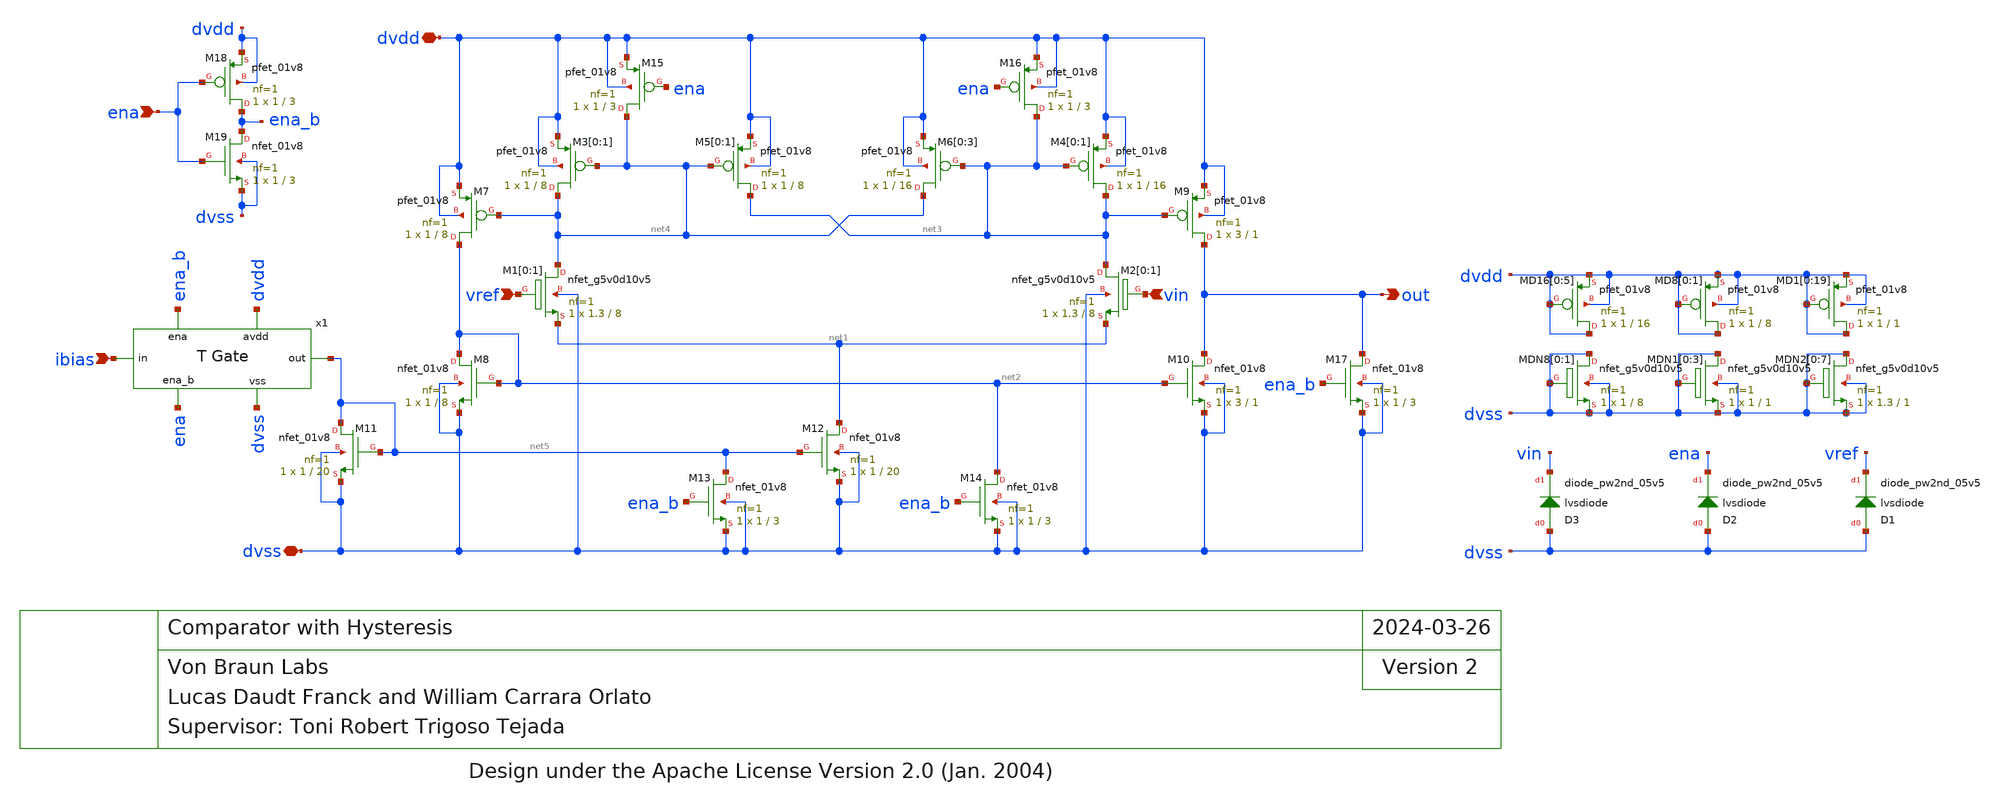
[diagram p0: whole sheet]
** sch_path: xschem/comp_hyst.sch
* Design under the Apache License Version 2.0 (Jan. 2004)
**.subckt comp_hyst dvdd vref vin out ibias ena dvss
*.iopin dvdd
*.ipin vref
*.ipin vin
*.opin out
*.ipin ibias
*.ipin ena
*.iopin dvss
XM5[0] net3 net4 dvdd dvdd sky130_fd_pr__pfet_01v8 L=8 W=1 nf=1 ad='int((nf+1)/2) * W/nf * 0.29' as='int((nf+2)/2) * W/nf * 0.29'
+ pd='2*int((nf+1)/2) * (W/nf + 0.29)' ps='2*int((nf+2)/2) * (W/nf + 0.29)' nrd='0.29 / W' nrs='0.29 / W'
+ sa=0 sb=0 sd=0 mult=1 m=1
XM5[1] net3 net4 dvdd dvdd sky130_fd_pr__pfet_01v8 L=8 W=1 nf=1 ad='int((nf+1)/2) * W/nf * 0.29' as='int((nf+2)/2) * W/nf * 0.29'
+ pd='2*int((nf+1)/2) * (W/nf + 0.29)' ps='2*int((nf+2)/2) * (W/nf + 0.29)' nrd='0.29 / W' nrs='0.29 / W'
+ sa=0 sb=0 sd=0 mult=1 m=1
XM3[0] net4 net4 dvdd dvdd sky130_fd_pr__pfet_01v8 L=8 W=1 nf=1 ad='int((nf+1)/2) * W/nf * 0.29' as='int((nf+2)/2) * W/nf * 0.29'
+ pd='2*int((nf+1)/2) * (W/nf + 0.29)' ps='2*int((nf+2)/2) * (W/nf + 0.29)' nrd='0.29 / W' nrs='0.29 / W'
+ sa=0 sb=0 sd=0 mult=1 m=1
XM3[1] net4 net4 dvdd dvdd sky130_fd_pr__pfet_01v8 L=8 W=1 nf=1 ad='int((nf+1)/2) * W/nf * 0.29' as='int((nf+2)/2) * W/nf * 0.29'
+ pd='2*int((nf+1)/2) * (W/nf + 0.29)' ps='2*int((nf+2)/2) * (W/nf + 0.29)' nrd='0.29 / W' nrs='0.29 / W'
+ sa=0 sb=0 sd=0 mult=1 m=1
XM7 net2 net4 dvdd dvdd sky130_fd_pr__pfet_01v8 L=8 W=1 nf=1 ad='int((nf+1)/2) * W/nf * 0.29' as='int((nf+2)/2) * W/nf * 0.29'
+ pd='2*int((nf+1)/2) * (W/nf + 0.29)' ps='2*int((nf+2)/2) * (W/nf + 0.29)' nrd='0.29 / W' nrs='0.29 / W'
+ sa=0 sb=0 sd=0 mult=1 m=1
XM4[0] net3 net3 dvdd dvdd sky130_fd_pr__pfet_01v8 L=16 W=1 nf=1 ad='int((nf+1)/2) * W/nf * 0.29' as='int((nf+2)/2) * W/nf * 0.29'
+ pd='2*int((nf+1)/2) * (W/nf + 0.29)' ps='2*int((nf+2)/2) * (W/nf + 0.29)' nrd='0.29 / W' nrs='0.29 / W'
+ sa=0 sb=0 sd=0 mult=1 m=1
XM4[1] net3 net3 dvdd dvdd sky130_fd_pr__pfet_01v8 L=16 W=1 nf=1 ad='int((nf+1)/2) * W/nf * 0.29' as='int((nf+2)/2) * W/nf * 0.29'
+ pd='2*int((nf+1)/2) * (W/nf + 0.29)' ps='2*int((nf+2)/2) * (W/nf + 0.29)' nrd='0.29 / W' nrs='0.29 / W'
+ sa=0 sb=0 sd=0 mult=1 m=1
XM11 net5 net5 dvss dvss sky130_fd_pr__nfet_01v8 L=20 W=1 nf=1 ad='int((nf+1)/2) * W/nf * 0.29' as='int((nf+2)/2) * W/nf * 0.29'
+ pd='2*int((nf+1)/2) * (W/nf + 0.29)' ps='2*int((nf+2)/2) * (W/nf + 0.29)' nrd='0.29 / W' nrs='0.29 / W'
+ sa=0 sb=0 sd=0 mult=1 m=1
XM12 net1 net5 dvss dvss sky130_fd_pr__nfet_01v8 L=20 W=1 nf=1 ad='int((nf+1)/2) * W/nf * 0.29' as='int((nf+2)/2) * W/nf * 0.29'
+ pd='2*int((nf+1)/2) * (W/nf + 0.29)' ps='2*int((nf+2)/2) * (W/nf + 0.29)' nrd='0.29 / W' nrs='0.29 / W'
+ sa=0 sb=0 sd=0 mult=1 m=1
XM9 out net3 dvdd dvdd sky130_fd_pr__pfet_01v8 L=1 W=3 nf=1 ad='int((nf+1)/2) * W/nf * 0.29' as='int((nf+2)/2) * W/nf * 0.29'
+ pd='2*int((nf+1)/2) * (W/nf + 0.29)' ps='2*int((nf+2)/2) * (W/nf + 0.29)' nrd='0.29 / W' nrs='0.29 / W'
+ sa=0 sb=0 sd=0 mult=1 m=1
XM10 out net2 dvss dvss sky130_fd_pr__nfet_01v8 L=1 W=3 nf=1 ad='int((nf+1)/2) * W/nf * 0.29' as='int((nf+2)/2) * W/nf * 0.29'
+ pd='2*int((nf+1)/2) * (W/nf + 0.29)' ps='2*int((nf+2)/2) * (W/nf + 0.29)' nrd='0.29 / W' nrs='0.29 / W'
+ sa=0 sb=0 sd=0 mult=1 m=1
XM17 out ena_b dvss dvss sky130_fd_pr__nfet_01v8 L=3 W=1 nf=1 ad='int((nf+1)/2) * W/nf * 0.29' as='int((nf+2)/2) * W/nf * 0.29'
+ pd='2*int((nf+1)/2) * (W/nf + 0.29)' ps='2*int((nf+2)/2) * (W/nf + 0.29)' nrd='0.29 / W' nrs='0.29 / W'
+ sa=0 sb=0 sd=0 mult=1 m=1
XM1[0] net4 vref net1 dvss sky130_fd_pr__nfet_g5v0d10v5 L=8 W=1.3 nf=1 ad='int((nf+1)/2) * W/nf * 0.29'
+ as='int((nf+2)/2) * W/nf * 0.29' pd='2*int((nf+1)/2) * (W/nf + 0.29)' ps='2*int((nf+2)/2) * (W/nf + 0.29)'
+ nrd='0.29 / W' nrs='0.29 / W' sa=0 sb=0 sd=0 mult=1 m=1
XM1[1] net4 vref net1 dvss sky130_fd_pr__nfet_g5v0d10v5 L=8 W=1.3 nf=1 ad='int((nf+1)/2) * W/nf * 0.29'
+ as='int((nf+2)/2) * W/nf * 0.29' pd='2*int((nf+1)/2) * (W/nf + 0.29)' ps='2*int((nf+2)/2) * (W/nf + 0.29)'
+ nrd='0.29 / W' nrs='0.29 / W' sa=0 sb=0 sd=0 mult=1 m=1
XM2[0] net3 vin net1 dvss sky130_fd_pr__nfet_g5v0d10v5 L=8 W=1.3 nf=1 ad='int((nf+1)/2) * W/nf * 0.29'
+ as='int((nf+2)/2) * W/nf * 0.29' pd='2*int((nf+1)/2) * (W/nf + 0.29)' ps='2*int((nf+2)/2) * (W/nf + 0.29)'
+ nrd='0.29 / W' nrs='0.29 / W' sa=0 sb=0 sd=0 mult=1 m=1
XM2[1] net3 vin net1 dvss sky130_fd_pr__nfet_g5v0d10v5 L=8 W=1.3 nf=1 ad='int((nf+1)/2) * W/nf * 0.29'
+ as='int((nf+2)/2) * W/nf * 0.29' pd='2*int((nf+1)/2) * (W/nf + 0.29)' ps='2*int((nf+2)/2) * (W/nf + 0.29)'
+ nrd='0.29 / W' nrs='0.29 / W' sa=0 sb=0 sd=0 mult=1 m=1
XM13 net5 ena_b dvss dvss sky130_fd_pr__nfet_01v8 L=3 W=1 nf=1 ad='int((nf+1)/2) * W/nf * 0.29' as='int((nf+2)/2) * W/nf * 0.29'
+ pd='2*int((nf+1)/2) * (W/nf + 0.29)' ps='2*int((nf+2)/2) * (W/nf + 0.29)' nrd='0.29 / W' nrs='0.29 / W'
+ sa=0 sb=0 sd=0 mult=1 m=1
XM6[0] net4 net3 dvdd dvdd sky130_fd_pr__pfet_01v8 L=16 W=1 nf=1 ad='int((nf+1)/2) * W/nf * 0.29' as='int((nf+2)/2) * W/nf * 0.29'
+ pd='2*int((nf+1)/2) * (W/nf + 0.29)' ps='2*int((nf+2)/2) * (W/nf + 0.29)' nrd='0.29 / W' nrs='0.29 / W'
+ sa=0 sb=0 sd=0 mult=1 m=1
XM6[1] net4 net3 dvdd dvdd sky130_fd_pr__pfet_01v8 L=16 W=1 nf=1 ad='int((nf+1)/2) * W/nf * 0.29' as='int((nf+2)/2) * W/nf * 0.29'
+ pd='2*int((nf+1)/2) * (W/nf + 0.29)' ps='2*int((nf+2)/2) * (W/nf + 0.29)' nrd='0.29 / W' nrs='0.29 / W'
+ sa=0 sb=0 sd=0 mult=1 m=1
XM6[2] net4 net3 dvdd dvdd sky130_fd_pr__pfet_01v8 L=16 W=1 nf=1 ad='int((nf+1)/2) * W/nf * 0.29' as='int((nf+2)/2) * W/nf * 0.29'
+ pd='2*int((nf+1)/2) * (W/nf + 0.29)' ps='2*int((nf+2)/2) * (W/nf + 0.29)' nrd='0.29 / W' nrs='0.29 / W'
+ sa=0 sb=0 sd=0 mult=1 m=1
XM6[3] net4 net3 dvdd dvdd sky130_fd_pr__pfet_01v8 L=16 W=1 nf=1 ad='int((nf+1)/2) * W/nf * 0.29' as='int((nf+2)/2) * W/nf * 0.29'
+ pd='2*int((nf+1)/2) * (W/nf + 0.29)' ps='2*int((nf+2)/2) * (W/nf + 0.29)' nrd='0.29 / W' nrs='0.29 / W'
+ sa=0 sb=0 sd=0 mult=1 m=1
XM8 net2 net2 dvss dvss sky130_fd_pr__nfet_01v8 L=8 W=1 nf=1 ad='int((nf+1)/2) * W/nf * 0.29' as='int((nf+2)/2) * W/nf * 0.29'
+ pd='2*int((nf+1)/2) * (W/nf + 0.29)' ps='2*int((nf+2)/2) * (W/nf + 0.29)' nrd='0.29 / W' nrs='0.29 / W'
+ sa=0 sb=0 sd=0 mult=1 m=1
XM16 net3 ena dvdd dvdd sky130_fd_pr__pfet_01v8 L=3 W=1 nf=1 ad='int((nf+1)/2) * W/nf * 0.29' as='int((nf+2)/2) * W/nf * 0.29'
+ pd='2*int((nf+1)/2) * (W/nf + 0.29)' ps='2*int((nf+2)/2) * (W/nf + 0.29)' nrd='0.29 / W' nrs='0.29 / W'
+ sa=0 sb=0 sd=0 mult=1 m=1
XM15 net4 ena dvdd dvdd sky130_fd_pr__pfet_01v8 L=3 W=1 nf=1 ad='int((nf+1)/2) * W/nf * 0.29' as='int((nf+2)/2) * W/nf * 0.29'
+ pd='2*int((nf+1)/2) * (W/nf + 0.29)' ps='2*int((nf+2)/2) * (W/nf + 0.29)' nrd='0.29 / W' nrs='0.29 / W'
+ sa=0 sb=0 sd=0 mult=1 m=1
XM14 net2 ena_b dvss dvss sky130_fd_pr__nfet_01v8 L=3 W=1 nf=1 ad='int((nf+1)/2) * W/nf * 0.29' as='int((nf+2)/2) * W/nf * 0.29'
+ pd='2*int((nf+1)/2) * (W/nf + 0.29)' ps='2*int((nf+2)/2) * (W/nf + 0.29)' nrd='0.29 / W' nrs='0.29 / W'
+ sa=0 sb=0 sd=0 mult=1 m=1
XM18 ena_b ena dvdd dvdd sky130_fd_pr__pfet_01v8 L=3 W=1 nf=1 ad='int((nf+1)/2) * W/nf * 0.29' as='int((nf+2)/2) * W/nf * 0.29'
+ pd='2*int((nf+1)/2) * (W/nf + 0.29)' ps='2*int((nf+2)/2) * (W/nf + 0.29)' nrd='0.29 / W' nrs='0.29 / W'
+ sa=0 sb=0 sd=0 mult=1 m=1
XM19 ena_b ena dvss dvss sky130_fd_pr__nfet_01v8 L=3 W=1 nf=1 ad='int((nf+1)/2) * W/nf * 0.29' as='int((nf+2)/2) * W/nf * 0.29'
+ pd='2*int((nf+1)/2) * (W/nf + 0.29)' ps='2*int((nf+2)/2) * (W/nf + 0.29)' nrd='0.29 / W' nrs='0.29 / W'
+ sa=0 sb=0 sd=0 mult=1 m=1
x1 ibias ena ena_b dvdd dvss net5 trans_gate
XMD16[0] dvdd dvdd dvdd dvdd sky130_fd_pr__pfet_01v8 L=16 W=1 nf=1 ad='int((nf+1)/2) * W/nf * 0.29' as='int((nf+2)/2) * W/nf * 0.29'
+ pd='2*int((nf+1)/2) * (W/nf + 0.29)' ps='2*int((nf+2)/2) * (W/nf + 0.29)' nrd='0.29 / W' nrs='0.29 / W'
+ sa=0 sb=0 sd=0 mult=1 m=1
XMD16[1] dvdd dvdd dvdd dvdd sky130_fd_pr__pfet_01v8 L=16 W=1 nf=1 ad='int((nf+1)/2) * W/nf * 0.29' as='int((nf+2)/2) * W/nf * 0.29'
+ pd='2*int((nf+1)/2) * (W/nf + 0.29)' ps='2*int((nf+2)/2) * (W/nf + 0.29)' nrd='0.29 / W' nrs='0.29 / W'
+ sa=0 sb=0 sd=0 mult=1 m=1
XMD16[2] dvdd dvdd dvdd dvdd sky130_fd_pr__pfet_01v8 L=16 W=1 nf=1 ad='int((nf+1)/2) * W/nf * 0.29' as='int((nf+2)/2) * W/nf * 0.29'
+ pd='2*int((nf+1)/2) * (W/nf + 0.29)' ps='2*int((nf+2)/2) * (W/nf + 0.29)' nrd='0.29 / W' nrs='0.29 / W'
+ sa=0 sb=0 sd=0 mult=1 m=1
XMD16[3] dvdd dvdd dvdd dvdd sky130_fd_pr__pfet_01v8 L=16 W=1 nf=1 ad='int((nf+1)/2) * W/nf * 0.29' as='int((nf+2)/2) * W/nf * 0.29'
+ pd='2*int((nf+1)/2) * (W/nf + 0.29)' ps='2*int((nf+2)/2) * (W/nf + 0.29)' nrd='0.29 / W' nrs='0.29 / W'
+ sa=0 sb=0 sd=0 mult=1 m=1
XMD16[4] dvdd dvdd dvdd dvdd sky130_fd_pr__pfet_01v8 L=16 W=1 nf=1 ad='int((nf+1)/2) * W/nf * 0.29' as='int((nf+2)/2) * W/nf * 0.29'
+ pd='2*int((nf+1)/2) * (W/nf + 0.29)' ps='2*int((nf+2)/2) * (W/nf + 0.29)' nrd='0.29 / W' nrs='0.29 / W'
+ sa=0 sb=0 sd=0 mult=1 m=1
XMD16[5] dvdd dvdd dvdd dvdd sky130_fd_pr__pfet_01v8 L=16 W=1 nf=1 ad='int((nf+1)/2) * W/nf * 0.29' as='int((nf+2)/2) * W/nf * 0.29'
+ pd='2*int((nf+1)/2) * (W/nf + 0.29)' ps='2*int((nf+2)/2) * (W/nf + 0.29)' nrd='0.29 / W' nrs='0.29 / W'
+ sa=0 sb=0 sd=0 mult=1 m=1
XMD8[0] dvdd dvdd dvdd dvdd sky130_fd_pr__pfet_01v8 L=8 W=1 nf=1 ad='int((nf+1)/2) * W/nf * 0.29' as='int((nf+2)/2) * W/nf * 0.29'
+ pd='2*int((nf+1)/2) * (W/nf + 0.29)' ps='2*int((nf+2)/2) * (W/nf + 0.29)' nrd='0.29 / W' nrs='0.29 / W'
+ sa=0 sb=0 sd=0 mult=1 m=1
XMD8[1] dvdd dvdd dvdd dvdd sky130_fd_pr__pfet_01v8 L=8 W=1 nf=1 ad='int((nf+1)/2) * W/nf * 0.29' as='int((nf+2)/2) * W/nf * 0.29'
+ pd='2*int((nf+1)/2) * (W/nf + 0.29)' ps='2*int((nf+2)/2) * (W/nf + 0.29)' nrd='0.29 / W' nrs='0.29 / W'
+ sa=0 sb=0 sd=0 mult=1 m=1
XMD1[0] dvdd dvdd dvdd dvdd sky130_fd_pr__pfet_01v8 L=1 W=1 nf=1 ad='int((nf+1)/2) * W/nf * 0.29' as='int((nf+2)/2) * W/nf * 0.29'
+ pd='2*int((nf+1)/2) * (W/nf + 0.29)' ps='2*int((nf+2)/2) * (W/nf + 0.29)' nrd='0.29 / W' nrs='0.29 / W'
+ sa=0 sb=0 sd=0 mult=1 m=1
XMD1[1] dvdd dvdd dvdd dvdd sky130_fd_pr__pfet_01v8 L=1 W=1 nf=1 ad='int((nf+1)/2) * W/nf * 0.29' as='int((nf+2)/2) * W/nf * 0.29'
+ pd='2*int((nf+1)/2) * (W/nf + 0.29)' ps='2*int((nf+2)/2) * (W/nf + 0.29)' nrd='0.29 / W' nrs='0.29 / W'
+ sa=0 sb=0 sd=0 mult=1 m=1
XMD1[2] dvdd dvdd dvdd dvdd sky130_fd_pr__pfet_01v8 L=1 W=1 nf=1 ad='int((nf+1)/2) * W/nf * 0.29' as='int((nf+2)/2) * W/nf * 0.29'
+ pd='2*int((nf+1)/2) * (W/nf + 0.29)' ps='2*int((nf+2)/2) * (W/nf + 0.29)' nrd='0.29 / W' nrs='0.29 / W'
+ sa=0 sb=0 sd=0 mult=1 m=1
XMD1[3] dvdd dvdd dvdd dvdd sky130_fd_pr__pfet_01v8 L=1 W=1 nf=1 ad='int((nf+1)/2) * W/nf * 0.29' as='int((nf+2)/2) * W/nf * 0.29'
+ pd='2*int((nf+1)/2) * (W/nf + 0.29)' ps='2*int((nf+2)/2) * (W/nf + 0.29)' nrd='0.29 / W' nrs='0.29 / W'
+ sa=0 sb=0 sd=0 mult=1 m=1
XMD1[4] dvdd dvdd dvdd dvdd sky130_fd_pr__pfet_01v8 L=1 W=1 nf=1 ad='int((nf+1)/2) * W/nf * 0.29' as='int((nf+2)/2) * W/nf * 0.29'
+ pd='2*int((nf+1)/2) * (W/nf + 0.29)' ps='2*int((nf+2)/2) * (W/nf + 0.29)' nrd='0.29 / W' nrs='0.29 / W'
+ sa=0 sb=0 sd=0 mult=1 m=1
XMD1[5] dvdd dvdd dvdd dvdd sky130_fd_pr__pfet_01v8 L=1 W=1 nf=1 ad='int((nf+1)/2) * W/nf * 0.29' as='int((nf+2)/2) * W/nf * 0.29'
+ pd='2*int((nf+1)/2) * (W/nf + 0.29)' ps='2*int((nf+2)/2) * (W/nf + 0.29)' nrd='0.29 / W' nrs='0.29 / W'
+ sa=0 sb=0 sd=0 mult=1 m=1
XMD1[6] dvdd dvdd dvdd dvdd sky130_fd_pr__pfet_01v8 L=1 W=1 nf=1 ad='int((nf+1)/2) * W/nf * 0.29' as='int((nf+2)/2) * W/nf * 0.29'
+ pd='2*int((nf+1)/2) * (W/nf + 0.29)' ps='2*int((nf+2)/2) * (W/nf + 0.29)' nrd='0.29 / W' nrs='0.29 / W'
+ sa=0 sb=0 sd=0 mult=1 m=1
XMD1[7] dvdd dvdd dvdd dvdd sky130_fd_pr__pfet_01v8 L=1 W=1 nf=1 ad='int((nf+1)/2) * W/nf * 0.29' as='int((nf+2)/2) * W/nf * 0.29'
+ pd='2*int((nf+1)/2) * (W/nf + 0.29)' ps='2*int((nf+2)/2) * (W/nf + 0.29)' nrd='0.29 / W' nrs='0.29 / W'
+ sa=0 sb=0 sd=0 mult=1 m=1
XMD1[8] dvdd dvdd dvdd dvdd sky130_fd_pr__pfet_01v8 L=1 W=1 nf=1 ad='int((nf+1)/2) * W/nf * 0.29' as='int((nf+2)/2) * W/nf * 0.29'
+ pd='2*int((nf+1)/2) * (W/nf + 0.29)' ps='2*int((nf+2)/2) * (W/nf + 0.29)' nrd='0.29 / W' nrs='0.29 / W'
+ sa=0 sb=0 sd=0 mult=1 m=1
XMD1[9] dvdd dvdd dvdd dvdd sky130_fd_pr__pfet_01v8 L=1 W=1 nf=1 ad='int((nf+1)/2) * W/nf * 0.29' as='int((nf+2)/2) * W/nf * 0.29'
+ pd='2*int((nf+1)/2) * (W/nf + 0.29)' ps='2*int((nf+2)/2) * (W/nf + 0.29)' nrd='0.29 / W' nrs='0.29 / W'
+ sa=0 sb=0 sd=0 mult=1 m=1
XMD1[10] dvdd dvdd dvdd dvdd sky130_fd_pr__pfet_01v8 L=1 W=1 nf=1 ad='int((nf+1)/2) * W/nf * 0.29' as='int((nf+2)/2) * W/nf * 0.29'
+ pd='2*int((nf+1)/2) * (W/nf + 0.29)' ps='2*int((nf+2)/2) * (W/nf + 0.29)' nrd='0.29 / W' nrs='0.29 / W'
+ sa=0 sb=0 sd=0 mult=1 m=1
XMD1[11] dvdd dvdd dvdd dvdd sky130_fd_pr__pfet_01v8 L=1 W=1 nf=1 ad='int((nf+1)/2) * W/nf * 0.29' as='int((nf+2)/2) * W/nf * 0.29'
+ pd='2*int((nf+1)/2) * (W/nf + 0.29)' ps='2*int((nf+2)/2) * (W/nf + 0.29)' nrd='0.29 / W' nrs='0.29 / W'
+ sa=0 sb=0 sd=0 mult=1 m=1
XMD1[12] dvdd dvdd dvdd dvdd sky130_fd_pr__pfet_01v8 L=1 W=1 nf=1 ad='int((nf+1)/2) * W/nf * 0.29' as='int((nf+2)/2) * W/nf * 0.29'
+ pd='2*int((nf+1)/2) * (W/nf + 0.29)' ps='2*int((nf+2)/2) * (W/nf + 0.29)' nrd='0.29 / W' nrs='0.29 / W'
+ sa=0 sb=0 sd=0 mult=1 m=1
XMD1[13] dvdd dvdd dvdd dvdd sky130_fd_pr__pfet_01v8 L=1 W=1 nf=1 ad='int((nf+1)/2) * W/nf * 0.29' as='int((nf+2)/2) * W/nf * 0.29'
+ pd='2*int((nf+1)/2) * (W/nf + 0.29)' ps='2*int((nf+2)/2) * (W/nf + 0.29)' nrd='0.29 / W' nrs='0.29 / W'
+ sa=0 sb=0 sd=0 mult=1 m=1
XMD1[14] dvdd dvdd dvdd dvdd sky130_fd_pr__pfet_01v8 L=1 W=1 nf=1 ad='int((nf+1)/2) * W/nf * 0.29' as='int((nf+2)/2) * W/nf * 0.29'
+ pd='2*int((nf+1)/2) * (W/nf + 0.29)' ps='2*int((nf+2)/2) * (W/nf + 0.29)' nrd='0.29 / W' nrs='0.29 / W'
+ sa=0 sb=0 sd=0 mult=1 m=1
XMD1[15] dvdd dvdd dvdd dvdd sky130_fd_pr__pfet_01v8 L=1 W=1 nf=1 ad='int((nf+1)/2) * W/nf * 0.29' as='int((nf+2)/2) * W/nf * 0.29'
+ pd='2*int((nf+1)/2) * (W/nf + 0.29)' ps='2*int((nf+2)/2) * (W/nf + 0.29)' nrd='0.29 / W' nrs='0.29 / W'
+ sa=0 sb=0 sd=0 mult=1 m=1
XMD1[16] dvdd dvdd dvdd dvdd sky130_fd_pr__pfet_01v8 L=1 W=1 nf=1 ad='int((nf+1)/2) * W/nf * 0.29' as='int((nf+2)/2) * W/nf * 0.29'
+ pd='2*int((nf+1)/2) * (W/nf + 0.29)' ps='2*int((nf+2)/2) * (W/nf + 0.29)' nrd='0.29 / W' nrs='0.29 / W'
+ sa=0 sb=0 sd=0 mult=1 m=1
XMD1[17] dvdd dvdd dvdd dvdd sky130_fd_pr__pfet_01v8 L=1 W=1 nf=1 ad='int((nf+1)/2) * W/nf * 0.29' as='int((nf+2)/2) * W/nf * 0.29'
+ pd='2*int((nf+1)/2) * (W/nf + 0.29)' ps='2*int((nf+2)/2) * (W/nf + 0.29)' nrd='0.29 / W' nrs='0.29 / W'
+ sa=0 sb=0 sd=0 mult=1 m=1
XMD1[18] dvdd dvdd dvdd dvdd sky130_fd_pr__pfet_01v8 L=1 W=1 nf=1 ad='int((nf+1)/2) * W/nf * 0.29' as='int((nf+2)/2) * W/nf * 0.29'
+ pd='2*int((nf+1)/2) * (W/nf + 0.29)' ps='2*int((nf+2)/2) * (W/nf + 0.29)' nrd='0.29 / W' nrs='0.29 / W'
+ sa=0 sb=0 sd=0 mult=1 m=1
XMD1[19] dvdd dvdd dvdd dvdd sky130_fd_pr__pfet_01v8 L=1 W=1 nf=1 ad='int((nf+1)/2) * W/nf * 0.29' as='int((nf+2)/2) * W/nf * 0.29'
+ pd='2*int((nf+1)/2) * (W/nf + 0.29)' ps='2*int((nf+2)/2) * (W/nf + 0.29)' nrd='0.29 / W' nrs='0.29 / W'
+ sa=0 sb=0 sd=0 mult=1 m=1
XMDN8[0] dvss dvss dvss dvss sky130_fd_pr__nfet_g5v0d10v5 L=8 W=1 nf=1 ad='int((nf+1)/2) * W/nf * 0.29'
+ as='int((nf+2)/2) * W/nf * 0.29' pd='2*int((nf+1)/2) * (W/nf + 0.29)' ps='2*int((nf+2)/2) * (W/nf + 0.29)'
+ nrd='0.29 / W' nrs='0.29 / W' sa=0 sb=0 sd=0 mult=1 m=1
XMDN8[1] dvss dvss dvss dvss sky130_fd_pr__nfet_g5v0d10v5 L=8 W=1 nf=1 ad='int((nf+1)/2) * W/nf * 0.29'
+ as='int((nf+2)/2) * W/nf * 0.29' pd='2*int((nf+1)/2) * (W/nf + 0.29)' ps='2*int((nf+2)/2) * (W/nf + 0.29)'
+ nrd='0.29 / W' nrs='0.29 / W' sa=0 sb=0 sd=0 mult=1 m=1
XMDN1[0] dvss dvss dvss dvss sky130_fd_pr__nfet_g5v0d10v5 L=1 W=1 nf=1 ad='int((nf+1)/2) * W/nf * 0.29'
+ as='int((nf+2)/2) * W/nf * 0.29' pd='2*int((nf+1)/2) * (W/nf + 0.29)' ps='2*int((nf+2)/2) * (W/nf + 0.29)'
+ nrd='0.29 / W' nrs='0.29 / W' sa=0 sb=0 sd=0 mult=1 m=1
XMDN1[1] dvss dvss dvss dvss sky130_fd_pr__nfet_g5v0d10v5 L=1 W=1 nf=1 ad='int((nf+1)/2) * W/nf * 0.29'
+ as='int((nf+2)/2) * W/nf * 0.29' pd='2*int((nf+1)/2) * (W/nf + 0.29)' ps='2*int((nf+2)/2) * (W/nf + 0.29)'
+ nrd='0.29 / W' nrs='0.29 / W' sa=0 sb=0 sd=0 mult=1 m=1
XMDN1[2] dvss dvss dvss dvss sky130_fd_pr__nfet_g5v0d10v5 L=1 W=1 nf=1 ad='int((nf+1)/2) * W/nf * 0.29'
+ as='int((nf+2)/2) * W/nf * 0.29' pd='2*int((nf+1)/2) * (W/nf + 0.29)' ps='2*int((nf+2)/2) * (W/nf + 0.29)'
+ nrd='0.29 / W' nrs='0.29 / W' sa=0 sb=0 sd=0 mult=1 m=1
XMDN1[3] dvss dvss dvss dvss sky130_fd_pr__nfet_g5v0d10v5 L=1 W=1 nf=1 ad='int((nf+1)/2) * W/nf * 0.29'
+ as='int((nf+2)/2) * W/nf * 0.29' pd='2*int((nf+1)/2) * (W/nf + 0.29)' ps='2*int((nf+2)/2) * (W/nf + 0.29)'
+ nrd='0.29 / W' nrs='0.29 / W' sa=0 sb=0 sd=0 mult=1 m=1
XMDN2[0] dvss dvss dvss dvss sky130_fd_pr__nfet_g5v0d10v5 L=1 W=1.3 nf=1 ad='int((nf+1)/2) * W/nf * 0.29'
+ as='int((nf+2)/2) * W/nf * 0.29' pd='2*int((nf+1)/2) * (W/nf + 0.29)' ps='2*int((nf+2)/2) * (W/nf + 0.29)'
+ nrd='0.29 / W' nrs='0.29 / W' sa=0 sb=0 sd=0 mult=1 m=1
XMDN2[1] dvss dvss dvss dvss sky130_fd_pr__nfet_g5v0d10v5 L=1 W=1.3 nf=1 ad='int((nf+1)/2) * W/nf * 0.29'
+ as='int((nf+2)/2) * W/nf * 0.29' pd='2*int((nf+1)/2) * (W/nf + 0.29)' ps='2*int((nf+2)/2) * (W/nf + 0.29)'
+ nrd='0.29 / W' nrs='0.29 / W' sa=0 sb=0 sd=0 mult=1 m=1
XMDN2[2] dvss dvss dvss dvss sky130_fd_pr__nfet_g5v0d10v5 L=1 W=1.3 nf=1 ad='int((nf+1)/2) * W/nf * 0.29'
+ as='int((nf+2)/2) * W/nf * 0.29' pd='2*int((nf+1)/2) * (W/nf + 0.29)' ps='2*int((nf+2)/2) * (W/nf + 0.29)'
+ nrd='0.29 / W' nrs='0.29 / W' sa=0 sb=0 sd=0 mult=1 m=1
XMDN2[3] dvss dvss dvss dvss sky130_fd_pr__nfet_g5v0d10v5 L=1 W=1.3 nf=1 ad='int((nf+1)/2) * W/nf * 0.29'
+ as='int((nf+2)/2) * W/nf * 0.29' pd='2*int((nf+1)/2) * (W/nf + 0.29)' ps='2*int((nf+2)/2) * (W/nf + 0.29)'
+ nrd='0.29 / W' nrs='0.29 / W' sa=0 sb=0 sd=0 mult=1 m=1
XMDN2[4] dvss dvss dvss dvss sky130_fd_pr__nfet_g5v0d10v5 L=1 W=1.3 nf=1 ad='int((nf+1)/2) * W/nf * 0.29'
+ as='int((nf+2)/2) * W/nf * 0.29' pd='2*int((nf+1)/2) * (W/nf + 0.29)' ps='2*int((nf+2)/2) * (W/nf + 0.29)'
+ nrd='0.29 / W' nrs='0.29 / W' sa=0 sb=0 sd=0 mult=1 m=1
XMDN2[5] dvss dvss dvss dvss sky130_fd_pr__nfet_g5v0d10v5 L=1 W=1.3 nf=1 ad='int((nf+1)/2) * W/nf * 0.29'
+ as='int((nf+2)/2) * W/nf * 0.29' pd='2*int((nf+1)/2) * (W/nf + 0.29)' ps='2*int((nf+2)/2) * (W/nf + 0.29)'
+ nrd='0.29 / W' nrs='0.29 / W' sa=0 sb=0 sd=0 mult=1 m=1
XMDN2[6] dvss dvss dvss dvss sky130_fd_pr__nfet_g5v0d10v5 L=1 W=1.3 nf=1 ad='int((nf+1)/2) * W/nf * 0.29'
+ as='int((nf+2)/2) * W/nf * 0.29' pd='2*int((nf+1)/2) * (W/nf + 0.29)' ps='2*int((nf+2)/2) * (W/nf + 0.29)'
+ nrd='0.29 / W' nrs='0.29 / W' sa=0 sb=0 sd=0 mult=1 m=1
XMDN2[7] dvss dvss dvss dvss sky130_fd_pr__nfet_g5v0d10v5 L=1 W=1.3 nf=1 ad='int((nf+1)/2) * W/nf * 0.29'
+ as='int((nf+2)/2) * W/nf * 0.29' pd='2*int((nf+1)/2) * (W/nf + 0.29)' ps='2*int((nf+2)/2) * (W/nf + 0.29)'
+ nrd='0.29 / W' nrs='0.29 / W' sa=0 sb=0 sd=0 mult=1 m=1
D3 dvss vin sky130_fd_pr__diode_pw2nd_05v5 area=0.315e12
D1 dvss vref sky130_fd_pr__diode_pw2nd_05v5 area=0.315e12
D2 dvss ena sky130_fd_pr__diode_pw2nd_05v5 area=0.315e12
**.ends

* expanding   symbol:  trans_gate.sym # of pins=6
** sym_path: blocks/comp_hyst/xschem/trans_gate.sym
** sch_path: blocks/comp_hyst/xschem/trans_gate.sch
.subckt trans_gate in ena_b ena avdd vss out
*.iopin avdd
*.iopin vss
*.ipin ena
*.ipin ena_b
*.ipin in
*.ipin out
XM1 in ena_b out vss sky130_fd_pr__nfet_g5v0d10v5 L=5 W=1 nf=1 ad='int((nf+1)/2) * W/nf * 0.29' as='int((nf+2)/2) * W/nf * 0.29'
+ pd='2*int((nf+1)/2) * (W/nf + 0.29)' ps='2*int((nf+2)/2) * (W/nf + 0.29)' nrd='0.29 / W' nrs='0.29 / W'
+ sa=0 sb=0 sd=0 mult=1 m=1
XM2 in ena out avdd sky130_fd_pr__pfet_g5v0d10v5 L=5 W=6 nf=1 ad='int((nf+1)/2) * W/nf * 0.29' as='int((nf+2)/2) * W/nf * 0.29'
+ pd='2*int((nf+1)/2) * (W/nf + 0.29)' ps='2*int((nf+2)/2) * (W/nf + 0.29)' nrd='0.29 / W' nrs='0.29 / W'
+ sa=0 sb=0 sd=0 mult=1 m=1
.ends

.end
